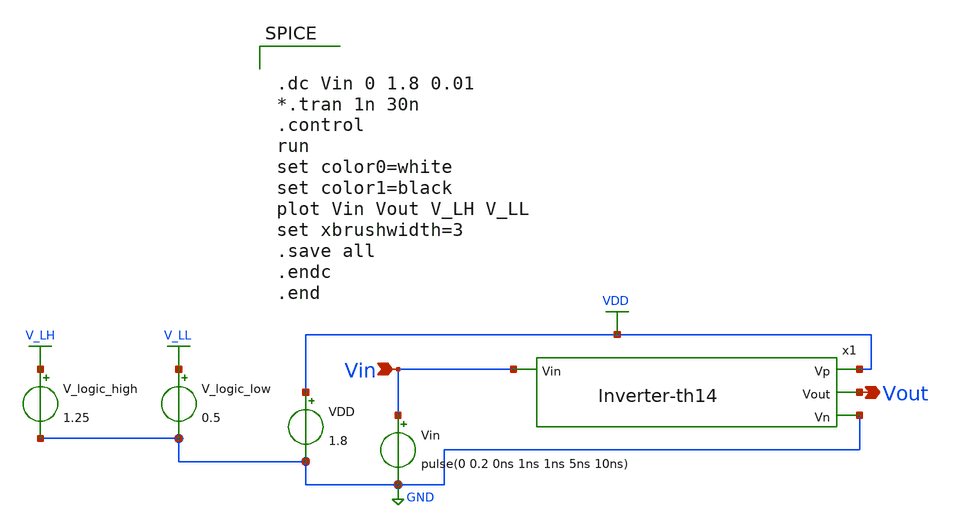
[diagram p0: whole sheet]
** sch_path: xschem/Vth_sch/Pre_layout/Inverter-th14.sch
**.subckt Inverter-th14 Vin Vout
*.ipin Vin
*.opin Vout
VDD VDD GND 1.8
Vin Vin GND pulse(0 0.2 0ns 1ns 1ns 5ns 10ns)
V_logic_high V_LH GND 1.25
V_logic_low V_LL GND 0.5
x1 VDD Vout Vin GND Inverter-th14
**** begin user architecture code


.lib /usr/local/share/pdk/sky130A/libs.tech/ngspice/sky130.lib.spice tt

.save all





.dc Vin 0 1.8 0.01
*.tran 1n 30n
.control
run
set color0=white
set color1=black
plot Vin Vout V_LH V_LL
set xbrushwidth=3
.save all
.endc
.end


**** end user architecture code
**.ends

* expanding   symbol:  /home/exotic/Desktop/ASIC_ADC/xschem/Vth_sch/Symbol/Inverter-th14.sym # of
*+ pins=4
** sym_path: xschem/Vth_sch/Symbol/Inverter-th14.sym
** sch_path: xschem/Vth_sch/Symbol/Inverter-th14.sch
.subckt Inverter-th14 Vp Vout Vin Vn
*.ipin Vin
*.opin Vout
*.opin Vp
*.opin Vn
XM1 Vout Vin Vp Vp sky130_fd_pr__pfet_01v8 L=0.15 W=19.5 nf=1 ad='int((nf+1)/2) * W/nf * 0.29' as='int((nf+2)/2) * W/nf * 0.29'
+ pd='2*int((nf+1)/2) * (W/nf + 0.29)' ps='2*int((nf+2)/2) * (W/nf + 0.29)' nrd='0.29 / W' nrs='0.29 / W'
+ sa=0 sb=0 sd=0 mult=1 m=1
XM3 Vout Vin net1 net1 sky130_fd_pr__nfet_01v8 L=19.5 W=0.36 nf=1 ad='int((nf+1)/2) * W/nf * 0.29' as='int((nf+2)/2) * W/nf * 0.29'
+ pd='2*int((nf+1)/2) * (W/nf + 0.29)' ps='2*int((nf+2)/2) * (W/nf + 0.29)' nrd='0.29 / W' nrs='0.29 / W'
+ sa=0 sb=0 sd=0 mult=1 m=1
XM2 Vn Vn net1 net1 sky130_fd_pr__pfet_01v8 L=0.15 W=1 nf=1 ad='int((nf+1)/2) * W/nf * 0.29' as='int((nf+2)/2) * W/nf * 0.29'
+ pd='2*int((nf+1)/2) * (W/nf + 0.29)' ps='2*int((nf+2)/2) * (W/nf + 0.29)' nrd='0.29 / W' nrs='0.29 / W'
+ sa=0 sb=0 sd=0 mult=1 m=1
.ends

.GLOBAL VDD
.GLOBAL GND
.GLOBAL V_LH
.GLOBAL V_LL
.end
